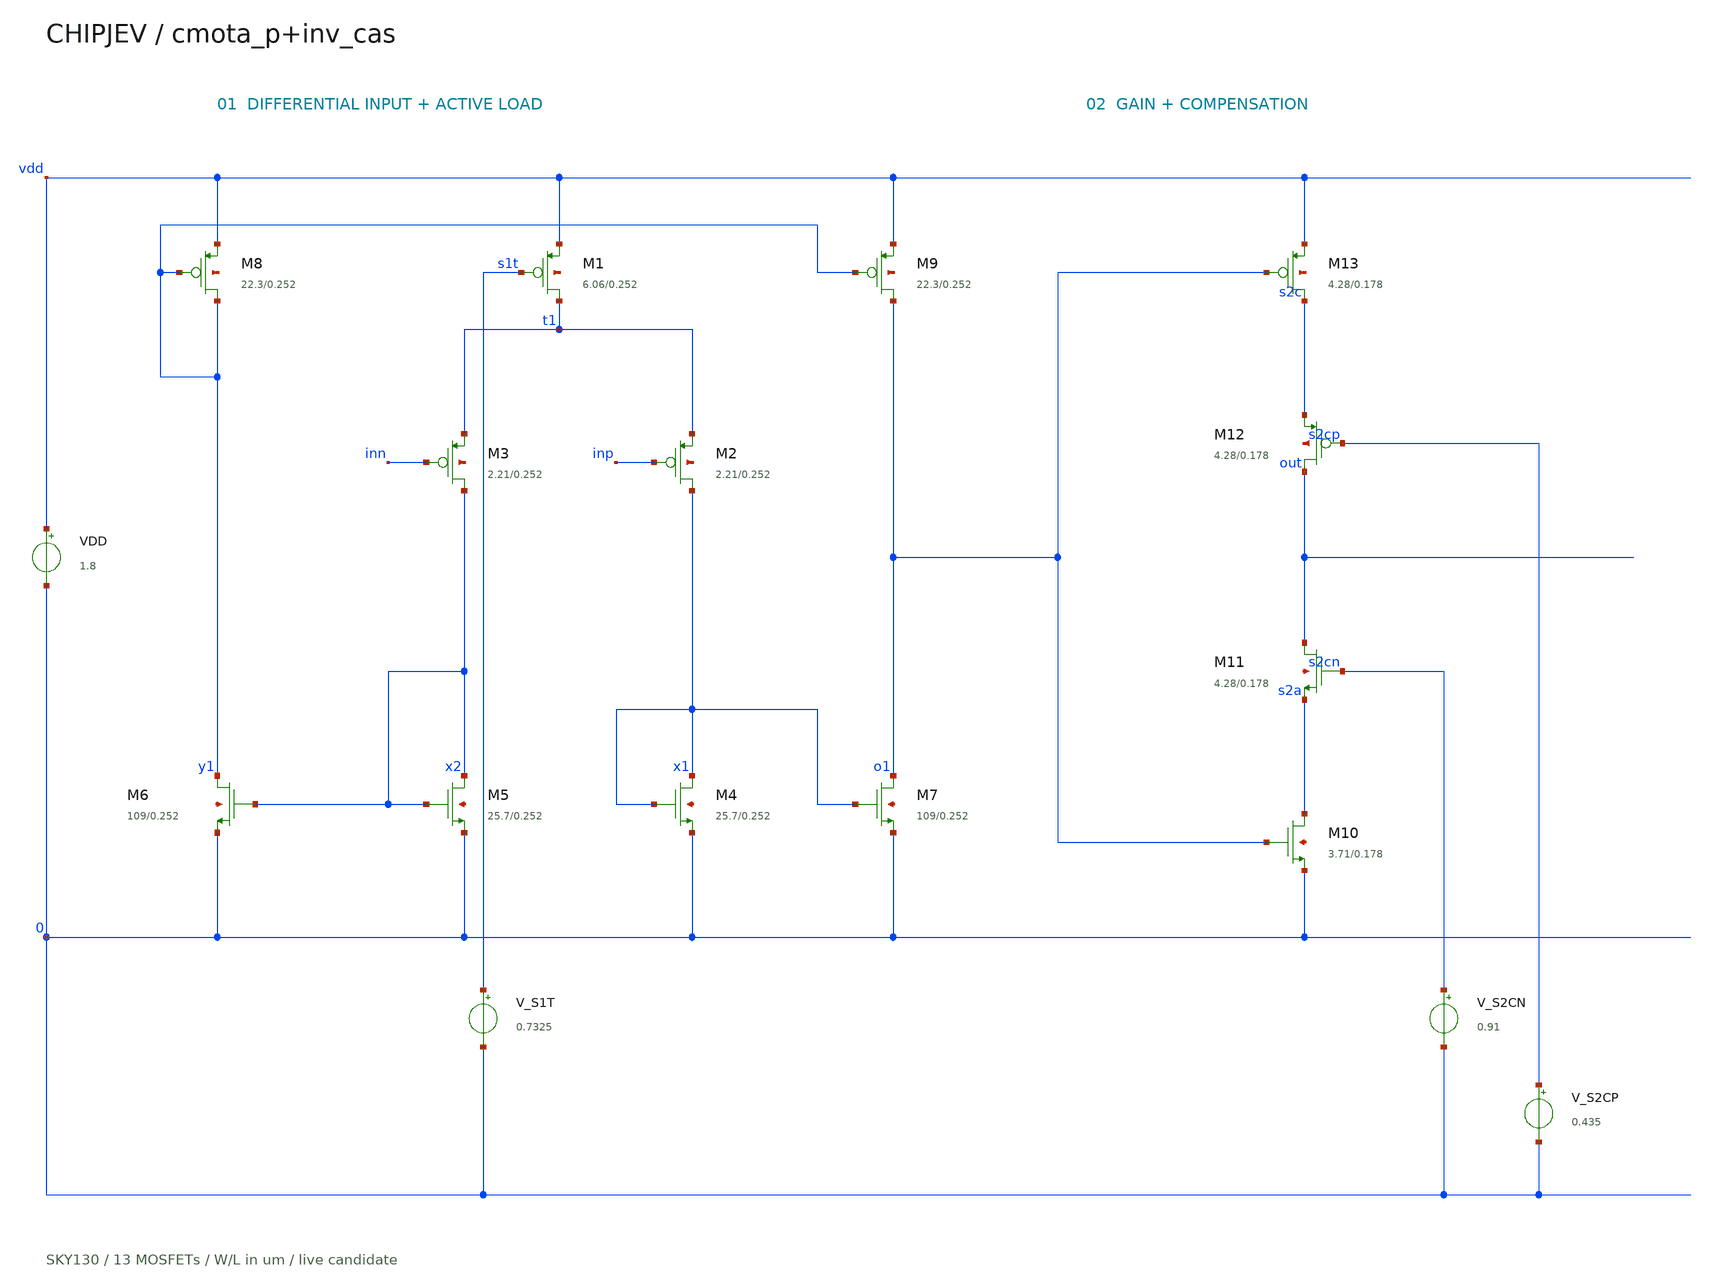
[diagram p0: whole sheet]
** sch_path: experiments/layout/results/opamp-gain/circuit.sch
**.subckt circuit
VDD vdd 0 1.8
XM1 t1 s1t vdd vdd sky130_fd_pr__pfet_01v8 L=0.252333 W=6.056 nf=1 ad=1.75624 as=1.75624 pd=12.692
+ ps=12.692 nrd=0.0478864 nrs=0.0478864 sa=0 sb=0 sd=0 mult=1 m=1
XM2 x1 inp t1 vdd sky130_fd_pr__pfet_01v8 L=0.252333 W=2.20539 nf=1 ad=0.639564 as=0.639564
+ pd=4.99079 ps=4.99079 nrd=0.131496 nrs=0.131496 sa=0 sb=0 sd=0 mult=1 m=1
XM3 x2 inn t1 vdd sky130_fd_pr__pfet_01v8 L=0.252333 W=2.20539 nf=1 ad=0.639564 as=0.639564
+ pd=4.99079 ps=4.99079 nrd=0.131496 nrs=0.131496 sa=0 sb=0 sd=0 mult=1 m=1
XM4 x1 x1 0 0 sky130_fd_pr__nfet_01v8 L=0.252333 W=25.738 nf=1 ad=7.46402 as=7.46402 pd=52.056
+ ps=52.056 nrd=0.0112674 nrs=0.0112674 sa=0 sb=0 sd=0 mult=1 m=1
XM5 x2 x2 0 0 sky130_fd_pr__nfet_01v8 L=0.252333 W=25.738 nf=1 ad=7.46402 as=7.46402 pd=52.056
+ ps=52.056 nrd=0.0112674 nrs=0.0112674 sa=0 sb=0 sd=0 mult=1 m=1
XM6 y1 x2 0 0 sky130_fd_pr__nfet_01v8 L=0.252333 W=109.26 nf=3 ad=21.1237 as=21.1237 pd=146.84
+ ps=146.84 nrd=0.00265421 nrs=0.00265421 sa=0 sb=0 sd=0 mult=1 m=1
XM7 o1 x1 0 0 sky130_fd_pr__nfet_01v8 L=0.252333 W=109.26 nf=3 ad=21.1237 as=21.1237 pd=146.84
+ ps=146.84 nrd=0.00265421 nrs=0.00265421 sa=0 sb=0 sd=0 mult=1 m=1
XM8 y1 y1 vdd vdd sky130_fd_pr__pfet_01v8 L=0.252333 W=22.281 nf=1 ad=6.4615 as=6.4615 pd=45.1421
+ ps=45.1421 nrd=0.0130156 nrs=0.0130156 sa=0 sb=0 sd=0 mult=1 m=1
XM9 o1 y1 vdd vdd sky130_fd_pr__pfet_01v8 L=0.252333 W=22.281 nf=1 ad=6.4615 as=6.4615 pd=45.1421
+ ps=45.1421 nrd=0.0130156 nrs=0.0130156 sa=0 sb=0 sd=0 mult=1 m=1
XM10 s2a o1 0 0 sky130_fd_pr__nfet_01v8 L=0.178333 W=3.70933 nf=1 ad=1.07571 as=1.07571 pd=7.99867
+ ps=7.99867 nrd=0.0781812 nrs=0.0781812 sa=0 sb=0 sd=0 mult=1 m=1
XM11 out s2cn s2a 0 sky130_fd_pr__nfet_01v8 L=0.178333 W=4.28 nf=1 ad=1.2412 as=1.2412 pd=9.14
+ ps=9.14 nrd=0.067757 nrs=0.067757 sa=0 sb=0 sd=0 mult=1 m=1
XM12 out s2cp s2c vdd sky130_fd_pr__pfet_01v8 L=0.178333 W=4.28 nf=1 ad=1.2412 as=1.2412 pd=9.14
+ ps=9.14 nrd=0.067757 nrs=0.067757 sa=0 sb=0 sd=0 mult=1 m=1
XM13 s2c o1 vdd vdd sky130_fd_pr__pfet_01v8 L=0.178333 W=4.28 nf=1 ad=1.2412 as=1.2412 pd=9.14
+ ps=9.14 nrd=0.067757 nrs=0.067757 sa=0 sb=0 sd=0 mult=1 m=1
V_S1T s1t 0 0.7325
V_S2CN s2cn 0 0.91
V_S2CP s2cp 0 0.435
**.ends
.end
